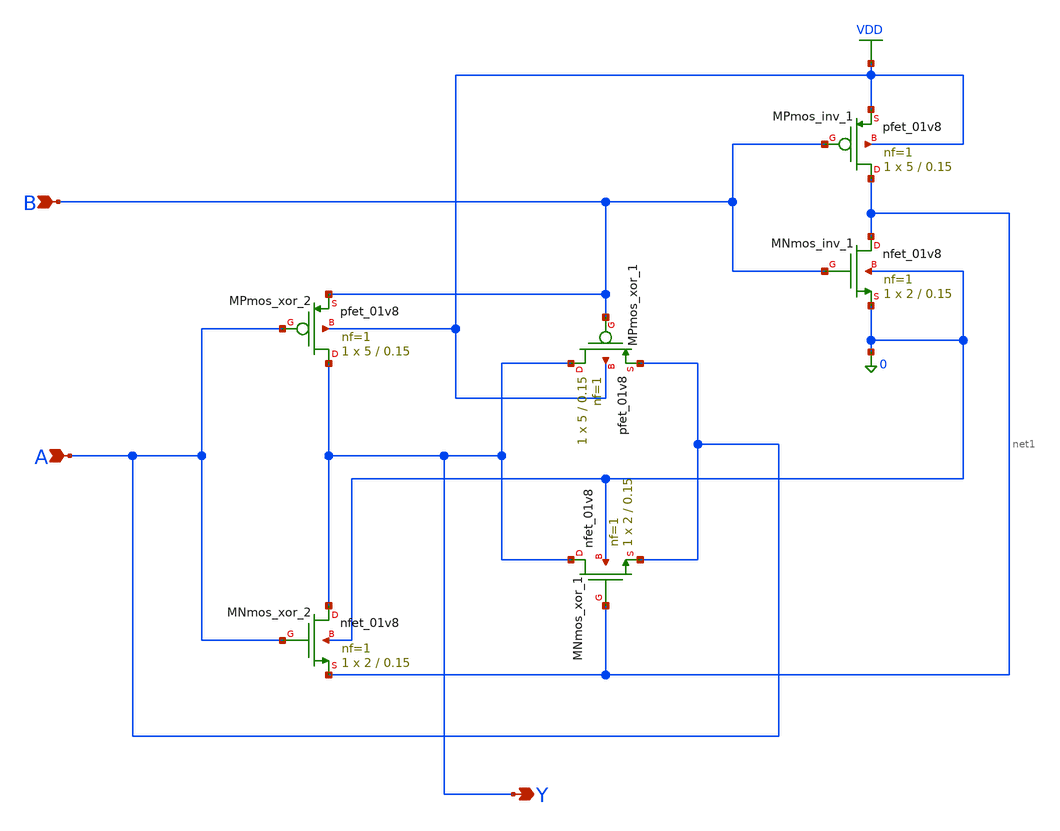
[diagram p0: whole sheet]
** sch_path: cells/full_adder_tg/xschem/xor2_design_khaosat.sch
**.subckt xor2_design_khaosat Y B A
*.opin Y
*.ipin B
*.ipin A
XMPmos_inv_1 net1 B VDD VDD sky130_fd_pr__pfet_01v8 L=0.15 W=5 nf=1 ad='int((1 + 1)/2) * 5 / 1 * 0.29'
+ as='int((1 + 2)/2) * 5 / 1 * 0.29' pd='2*int((1 + 1)/2) * (5 / 1 + 0.29)' ps='2*int((1 + 2)/2) * (5 / 1 + 0.29)'
+ nrd='0.29 / 5 ' nrs='0.29 / 5 ' sa=0 sb=0 sd=0 mult=1 m=1
XMNmos_inv_1 net1 B 0 0 sky130_fd_pr__nfet_01v8 L=0.15 W=2 nf=1 ad='int((1 + 1)/2) * 2 / 1 * 0.29' as='int((1 + 2)/2) * 2 / 1 * 0.29'
+ pd='2*int((1 + 1)/2) * (2 / 1 + 0.29)' ps='2*int((1 + 2)/2) * (2 / 1 + 0.29)' nrd='0.29 / 2 ' nrs='0.29 / 2 '
+ sa=0 sb=0 sd=0 mult=1 m=1
XMPmos_xor_1 Y B A VDD sky130_fd_pr__pfet_01v8 L=0.15 W=5 nf=1 ad='int((1 + 1)/2) * 5 / 1 * 0.29' as='int((1 + 2)/2) * 5 / 1 * 0.29'
+ pd='2*int((1 + 1)/2) * (5 / 1 + 0.29)' ps='2*int((1 + 2)/2) * (5 / 1 + 0.29)' nrd='0.29 / 5 ' nrs='0.29 / 5 '
+ sa=0 sb=0 sd=0 mult=1 m=1
XMNmos_xor_1 Y net1 A 0 sky130_fd_pr__nfet_01v8 L=0.15 W=2 nf=1 ad='int((1 + 1)/2) * 2 / 1 * 0.29' as='int((1 + 2)/2) * 2 / 1 * 0.29'
+ pd='2*int((1 + 1)/2) * (2 / 1 + 0.29)' ps='2*int((1 + 2)/2) * (2 / 1 + 0.29)' nrd='0.29 / 2 ' nrs='0.29 / 2 '
+ sa=0 sb=0 sd=0 mult=1 m=1
XMPmos_xor_2 Y A B VDD sky130_fd_pr__pfet_01v8 L=0.15 W=5 nf=1 ad='int((1 + 1)/2) * 5 / 1 * 0.29' as='int((1 + 2)/2) * 5 / 1 * 0.29'
+ pd='2*int((1 + 1)/2) * (5 / 1 + 0.29)' ps='2*int((1 + 2)/2) * (5 / 1 + 0.29)' nrd='0.29 / 5 ' nrs='0.29 / 5 '
+ sa=0 sb=0 sd=0 mult=1 m=1
XMNmos_xor_2 Y A net1 0 sky130_fd_pr__nfet_01v8 L=0.15 W=2 nf=1 ad='int((1 + 1)/2) * 2 / 1 * 0.29' as='int((1 + 2)/2) * 2 / 1 * 0.29'
+ pd='2*int((1 + 1)/2) * (2 / 1 + 0.29)' ps='2*int((1 + 2)/2) * (2 / 1 + 0.29)' nrd='0.29 / 2 ' nrs='0.29 / 2 '
+ sa=0 sb=0 sd=0 mult=1 m=1
**.ends
.GLOBAL VDD
.end
